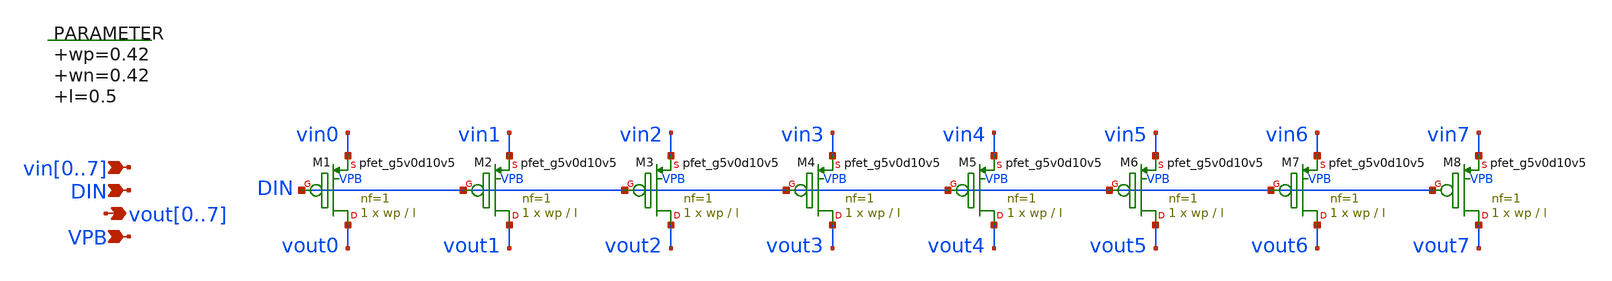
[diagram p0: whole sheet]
** sch_path: xschem/switch_pmos_1g_8o.sch
**.subckt switch_pmos_1g_8o vin0,vin1,vin2,vin3,vin4,vin5,vin6,vin7
*+ vout0,vout1,vout2,vout3,vout4,vout5,vout6,vout7 VPB DIN
*.ipin vin0,vin1,vin2,vin3,vin4,vin5,vin6,vin7
*.opin vout0,vout1,vout2,vout3,vout4,vout5,vout6,vout7
*.ipin VPB
*.ipin DIN
.param wp=0.42 wn=0.42 l=0.5

XM1 vout0 DIN vin0 VPB sky130_fd_pr__pfet_g5v0d10v5 L=l W=wp nf=1 ad='int((nf+1)/2) * W/nf * 0.29' as='int((nf+2)/2) * W/nf * 0.29'
+ pd='2*int((nf+1)/2) * (W/nf + 0.29)' ps='2*int((nf+2)/2) * (W/nf + 0.29)' nrd='0.29 / W' nrs='0.29 / W'
+ sa=0 sb=0 sd=0 mult=1 m=1
XM2 vout1 DIN vin1 VPB sky130_fd_pr__pfet_g5v0d10v5 L=l W=wp nf=1 ad='int((nf+1)/2) * W/nf * 0.29' as='int((nf+2)/2) * W/nf * 0.29'
+ pd='2*int((nf+1)/2) * (W/nf + 0.29)' ps='2*int((nf+2)/2) * (W/nf + 0.29)' nrd='0.29 / W' nrs='0.29 / W'
+ sa=0 sb=0 sd=0 mult=1 m=1
XM3 vout2 DIN vin2 VPB sky130_fd_pr__pfet_g5v0d10v5 L=l W=wp nf=1 ad='int((nf+1)/2) * W/nf * 0.29' as='int((nf+2)/2) * W/nf * 0.29'
+ pd='2*int((nf+1)/2) * (W/nf + 0.29)' ps='2*int((nf+2)/2) * (W/nf + 0.29)' nrd='0.29 / W' nrs='0.29 / W'
+ sa=0 sb=0 sd=0 mult=1 m=1
XM4 vout3 DIN vin3 VPB sky130_fd_pr__pfet_g5v0d10v5 L=l W=wp nf=1 ad='int((nf+1)/2) * W/nf * 0.29' as='int((nf+2)/2) * W/nf * 0.29'
+ pd='2*int((nf+1)/2) * (W/nf + 0.29)' ps='2*int((nf+2)/2) * (W/nf + 0.29)' nrd='0.29 / W' nrs='0.29 / W'
+ sa=0 sb=0 sd=0 mult=1 m=1
XM5 vout4 DIN vin4 VPB sky130_fd_pr__pfet_g5v0d10v5 L=l W=wp nf=1 ad='int((nf+1)/2) * W/nf * 0.29' as='int((nf+2)/2) * W/nf * 0.29'
+ pd='2*int((nf+1)/2) * (W/nf + 0.29)' ps='2*int((nf+2)/2) * (W/nf + 0.29)' nrd='0.29 / W' nrs='0.29 / W'
+ sa=0 sb=0 sd=0 mult=1 m=1
XM6 vout5 DIN vin5 VPB sky130_fd_pr__pfet_g5v0d10v5 L=l W=wp nf=1 ad='int((nf+1)/2) * W/nf * 0.29' as='int((nf+2)/2) * W/nf * 0.29'
+ pd='2*int((nf+1)/2) * (W/nf + 0.29)' ps='2*int((nf+2)/2) * (W/nf + 0.29)' nrd='0.29 / W' nrs='0.29 / W'
+ sa=0 sb=0 sd=0 mult=1 m=1
XM7 vout6 DIN vin6 VPB sky130_fd_pr__pfet_g5v0d10v5 L=l W=wp nf=1 ad='int((nf+1)/2) * W/nf * 0.29' as='int((nf+2)/2) * W/nf * 0.29'
+ pd='2*int((nf+1)/2) * (W/nf + 0.29)' ps='2*int((nf+2)/2) * (W/nf + 0.29)' nrd='0.29 / W' nrs='0.29 / W'
+ sa=0 sb=0 sd=0 mult=1 m=1
XM8 vout7 DIN vin7 VPB sky130_fd_pr__pfet_g5v0d10v5 L=l W=wp nf=1 ad='int((nf+1)/2) * W/nf * 0.29' as='int((nf+2)/2) * W/nf * 0.29'
+ pd='2*int((nf+1)/2) * (W/nf + 0.29)' ps='2*int((nf+2)/2) * (W/nf + 0.29)' nrd='0.29 / W' nrs='0.29 / W'
+ sa=0 sb=0 sd=0 mult=1 m=1
**.ends
.end
